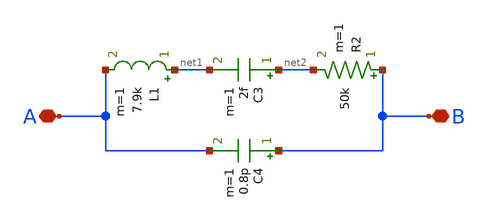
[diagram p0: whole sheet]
** sch_path: member_project/JJY_Receiver/Masahiro/jjy_recv/XTALOSC/XTAL_model.sch
**.subckt XTAL_model B A
*.iopin B
*.iopin A
L1 net1 A 7.9k m=1
C3 net2 net1 2f m=1
R2 B net2 50k m=1
C4 B A 0.8p m=1
**.ends
.end
